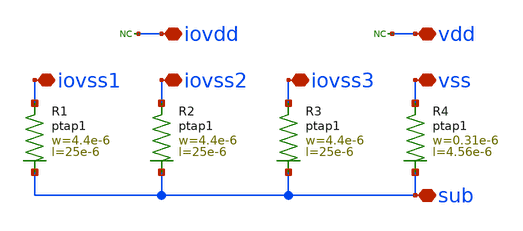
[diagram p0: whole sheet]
** sch_path: MSPHY6034-main/schematic/xschem/openpdk-libraries/ihp-sg13g2/sg13g2_io/xschem/sg13g2_Filler1000.sch
**.subckt sg13g2_Filler1000 iovss1 iovss2 iovss3 vss iovdd vdd sub
*.iopin iovss1
*.iopin iovss2
*.iopin iovss3
*.iopin vss
*.iopin iovdd
*.iopin vdd
*.iopin sub
XR3 iovss3 sub ptap1 R=5.806 w=4.4e-6 l=25e-6
XR4 vss sub ptap1 R=87.86 w=0.31e-6 l=4.56e-6
* noconn iovdd
* noconn vdd
XR1 iovss1 sub ptap1 R=5.806 w=4.4e-6 l=25e-6
XR2 iovss2 sub ptap1 R=5.806 w=4.4e-6 l=25e-6
**.ends
.end
